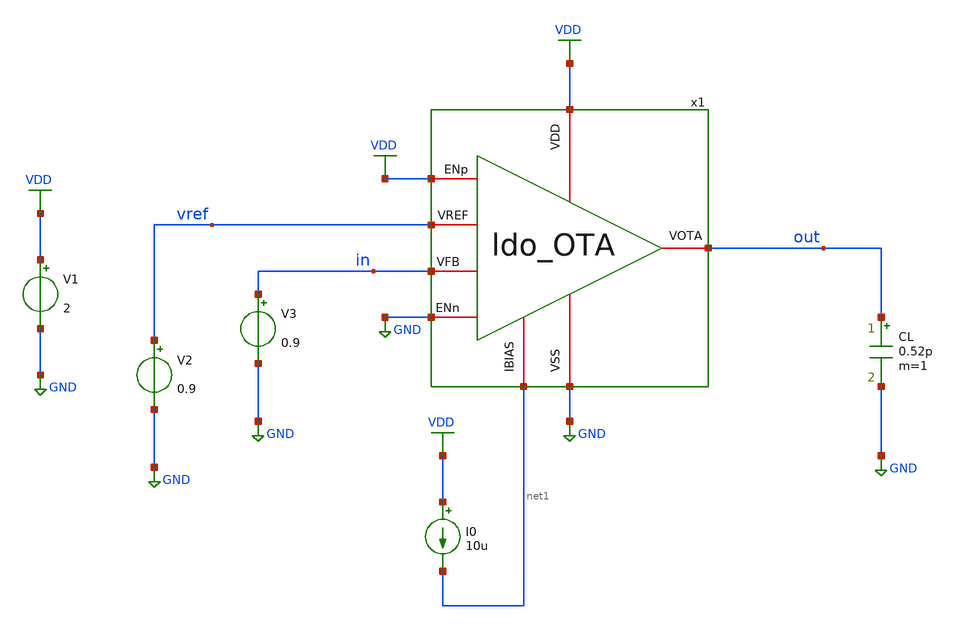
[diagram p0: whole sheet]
** sch_path: designs/libs/tb_ldo/tb_ldo_OTA_ac/tb_ldo_OTA_ac.sch
**.subckt tb_ldo_OTA_ac
V1 VDD GND 2
V2 vref GND 0.9
I0 VDD net1 10u
CL out GND 0.52p m=1
V3 in GND 0.9
x1 VDD vref in out net1 GND VDD GND ldo_OTA
**** begin user architecture code



.control
save all

** Set sources
alter @V3[AC] = 1

** Simulations
ac dec 100 1 10G

** Plots
setplot ac1
let gain_db = db(v(out))
plot gain_db
let phase_deg = cph(v(out))*180/pi
plot phase_deg

** Measurements
meas ac DC_gain FIND gain_db AT=1Hz
let gain_3db = DC_gain-3
meas ac f_3db WHEN gain_db=$&gain_3db
meas ac f_0db WHEN gain_db=0
meas ac phase_0db FIND phase_deg WHEN gain_db=0
let phase_margin = 180 + phase_0db
print phase_margin

write tb_ldo_OTA_ac.raw

.endc
* ngspice commands




.include $::180MCU_MODELS/design.ngspice
.lib $::180MCU_MODELS/sm141064.ngspice typical
.lib $::180MCU_MODELS/sm141064.ngspice cap_mim
.lib $::180MCU_MODELS/sm141064.ngspice moscap_typical
.lib $::180MCU_MODELS/sm141064.ngspice mimcap_typical
.lib $::180MCU_MODELS/sm141064.ngspice res_typical
* .lib $::180MCU_MODELS/sm141064.ngspice res_statistical
* ngspice commands

**** end user architecture code
**.ends

* expanding   symbol:  libs/core_ldo/ldo_OTA/ldo_OTA.sym # of pins=8
** sym_path: designs/libs/core_ldo/ldo_OTA/ldo_OTA.sym
** sch_path: designs/libs/core_ldo/ldo_OTA/ldo_OTA.sch
.subckt ldo_OTA VDD VREF VFB VOTA IBIAS VSS ENp ENn
*.iopin VDD
*.iopin VSS
*.iopin VOTA
*.iopin VREF
*.iopin IBIAS
*.iopin VFB
*.ipin ENp
*.ipin ENn
XM3 Vbp1 Vbp1 VDD VDD pfet_05v0 L=1.00u W=5.50u nf=1 ad='int((nf+1)/2) * W/nf * 0.18u' as='int((nf+2)/2) * W/nf * 0.18u'
+ pd='2*int((nf+1)/2) * (W/nf + 0.18u)' ps='2*int((nf+2)/2) * (W/nf + 0.18u)' nrd='0.18u / W' nrs='0.18u / W'
+ sa=0 sb=0 sd=0 m=2
XM4 Vbp2 Vbp2 VDD VDD pfet_05v0 L=1.00u W=5.50u nf=1 ad='int((nf+1)/2) * W/nf * 0.18u' as='int((nf+2)/2) * W/nf * 0.18u'
+ pd='2*int((nf+1)/2) * (W/nf + 0.18u)' ps='2*int((nf+2)/2) * (W/nf + 0.18u)' nrd='0.18u / W' nrs='0.18u / W'
+ sa=0 sb=0 sd=0 m=2
XM5 Vbn2 Vbp1 VDD VDD pfet_05v0 L=1.00u W=5.50u nf=1 ad='int((nf+1)/2) * W/nf * 0.18u' as='int((nf+2)/2) * W/nf * 0.18u'
+ pd='2*int((nf+1)/2) * (W/nf + 0.18u)' ps='2*int((nf+2)/2) * (W/nf + 0.18u)' nrd='0.18u / W' nrs='0.18u / W'
+ sa=0 sb=0 sd=0 m=2
XM6 VOTA Vbp2 VDD VDD pfet_05v0 L=1.00u W=5.50u nf=1 ad='int((nf+1)/2) * W/nf * 0.18u' as='int((nf+2)/2) * W/nf * 0.18u'
+ pd='2*int((nf+1)/2) * (W/nf + 0.18u)' ps='2*int((nf+2)/2) * (W/nf + 0.18u)' nrd='0.18u / W' nrs='0.18u / W'
+ sa=0 sb=0 sd=0 m=6
XM9 Vbn1 Vbn1 VSS VSS nfet_05v0 L=1.00u W=3.00u nf=1 ad='int((nf+1)/2) * W/nf * 0.18u' as='int((nf+2)/2) * W/nf * 0.18u'
+ pd='2*int((nf+1)/2) * (W/nf + 0.18u)' ps='2*int((nf+2)/2) * (W/nf + 0.18u)' nrd='0.18u / W' nrs='0.18u / W'
+ sa=0 sb=0 sd=0 m=2
XM10 Vtail Vbn1 VSS VSS nfet_05v0 L=1.00u W=3.00u nf=1 ad='int((nf+1)/2) * W/nf * 0.18u' as='int((nf+2)/2) * W/nf * 0.18u'
+ pd='2*int((nf+1)/2) * (W/nf + 0.18u)' ps='2*int((nf+2)/2) * (W/nf + 0.18u)' nrd='0.18u / W' nrs='0.18u / W'
+ sa=0 sb=0 sd=0 m=2
XM7 Vbn2 Vbn2 VSS VSS nfet_05v0 L=1.00u W=1.25u nf=1 ad='int((nf+1)/2) * W/nf * 0.18u' as='int((nf+2)/2) * W/nf * 0.18u'
+ pd='2*int((nf+1)/2) * (W/nf + 0.18u)' ps='2*int((nf+2)/2) * (W/nf + 0.18u)' nrd='0.18u / W' nrs='0.18u / W'
+ sa=0 sb=0 sd=0 m=2
XM8 VOTA Vbn2 VSS VSS nfet_05v0 L=1.00u W=1.25u nf=1 ad='int((nf+1)/2) * W/nf * 0.18u' as='int((nf+2)/2) * W/nf * 0.18u'
+ pd='2*int((nf+1)/2) * (W/nf + 0.18u)' ps='2*int((nf+2)/2) * (W/nf + 0.18u)' nrd='0.18u / W' nrs='0.18u / W'
+ sa=0 sb=0 sd=0 m=6
XM1 Vbp1 VREF Vtail VSS nfet_05v0 L=0.60u W=5.00u nf=1 ad='int((nf+1)/2) * W/nf * 0.18u' as='int((nf+2)/2) * W/nf * 0.18u'
+ pd='2*int((nf+1)/2) * (W/nf + 0.18u)' ps='2*int((nf+2)/2) * (W/nf + 0.18u)' nrd='0.18u / W' nrs='0.18u / W'
+ sa=0 sb=0 sd=0 m=14
XM2 Vbp2 VFB Vtail VSS nfet_05v0 L=0.60u W=5.00u nf=1 ad='int((nf+1)/2) * W/nf * 0.18u' as='int((nf+2)/2) * W/nf * 0.18u'
+ pd='2*int((nf+1)/2) * (W/nf + 0.18u)' ps='2*int((nf+2)/2) * (W/nf + 0.18u)' nrd='0.18u / W' nrs='0.18u / W'
+ sa=0 sb=0 sd=0 m=14
XMpota_dummy_L[3] VDD VDD VDD VDD pfet_05v0 L=1.00u W=5.50u nf=1 ad='int((nf+1)/2) * W/nf * 0.18u' as='int((nf+2)/2) * W/nf * 0.18u'
+ pd='2*int((nf+1)/2) * (W/nf + 0.18u)' ps='2*int((nf+2)/2) * (W/nf + 0.18u)' nrd='0.18u / W' nrs='0.18u / W'
+ sa=0 sb=0 sd=0 m=1
XMpota_dummy_L[2] VDD VDD VDD VDD pfet_05v0 L=1.00u W=5.50u nf=1 ad='int((nf+1)/2) * W/nf * 0.18u' as='int((nf+2)/2) * W/nf * 0.18u'
+ pd='2*int((nf+1)/2) * (W/nf + 0.18u)' ps='2*int((nf+2)/2) * (W/nf + 0.18u)' nrd='0.18u / W' nrs='0.18u / W'
+ sa=0 sb=0 sd=0 m=1
XMpota_dummy_L[1] VDD VDD VDD VDD pfet_05v0 L=1.00u W=5.50u nf=1 ad='int((nf+1)/2) * W/nf * 0.18u' as='int((nf+2)/2) * W/nf * 0.18u'
+ pd='2*int((nf+1)/2) * (W/nf + 0.18u)' ps='2*int((nf+2)/2) * (W/nf + 0.18u)' nrd='0.18u / W' nrs='0.18u / W'
+ sa=0 sb=0 sd=0 m=1
XMpota_dummy_L[0] VDD VDD VDD VDD pfet_05v0 L=1.00u W=5.50u nf=1 ad='int((nf+1)/2) * W/nf * 0.18u' as='int((nf+2)/2) * W/nf * 0.18u'
+ pd='2*int((nf+1)/2) * (W/nf + 0.18u)' ps='2*int((nf+2)/2) * (W/nf + 0.18u)' nrd='0.18u / W' nrs='0.18u / W'
+ sa=0 sb=0 sd=0 m=1
XMpota_dummy_TB[15] VDD VDD VDD VDD pfet_05v0 L=1.00u W=5.50u nf=1 ad='int((nf+1)/2) * W/nf * 0.18u'
+ as='int((nf+2)/2) * W/nf * 0.18u' pd='2*int((nf+1)/2) * (W/nf + 0.18u)' ps='2*int((nf+2)/2) * (W/nf + 0.18u)'
+ nrd='0.18u / W' nrs='0.18u / W' sa=0 sb=0 sd=0 m=1
XMpota_dummy_TB[14] VDD VDD VDD VDD pfet_05v0 L=1.00u W=5.50u nf=1 ad='int((nf+1)/2) * W/nf * 0.18u'
+ as='int((nf+2)/2) * W/nf * 0.18u' pd='2*int((nf+1)/2) * (W/nf + 0.18u)' ps='2*int((nf+2)/2) * (W/nf + 0.18u)'
+ nrd='0.18u / W' nrs='0.18u / W' sa=0 sb=0 sd=0 m=1
XMpota_dummy_TB[13] VDD VDD VDD VDD pfet_05v0 L=1.00u W=5.50u nf=1 ad='int((nf+1)/2) * W/nf * 0.18u'
+ as='int((nf+2)/2) * W/nf * 0.18u' pd='2*int((nf+1)/2) * (W/nf + 0.18u)' ps='2*int((nf+2)/2) * (W/nf + 0.18u)'
+ nrd='0.18u / W' nrs='0.18u / W' sa=0 sb=0 sd=0 m=1
XMpota_dummy_TB[12] VDD VDD VDD VDD pfet_05v0 L=1.00u W=5.50u nf=1 ad='int((nf+1)/2) * W/nf * 0.18u'
+ as='int((nf+2)/2) * W/nf * 0.18u' pd='2*int((nf+1)/2) * (W/nf + 0.18u)' ps='2*int((nf+2)/2) * (W/nf + 0.18u)'
+ nrd='0.18u / W' nrs='0.18u / W' sa=0 sb=0 sd=0 m=1
XMpota_dummy_TB[11] VDD VDD VDD VDD pfet_05v0 L=1.00u W=5.50u nf=1 ad='int((nf+1)/2) * W/nf * 0.18u'
+ as='int((nf+2)/2) * W/nf * 0.18u' pd='2*int((nf+1)/2) * (W/nf + 0.18u)' ps='2*int((nf+2)/2) * (W/nf + 0.18u)'
+ nrd='0.18u / W' nrs='0.18u / W' sa=0 sb=0 sd=0 m=1
XMpota_dummy_TB[10] VDD VDD VDD VDD pfet_05v0 L=1.00u W=5.50u nf=1 ad='int((nf+1)/2) * W/nf * 0.18u'
+ as='int((nf+2)/2) * W/nf * 0.18u' pd='2*int((nf+1)/2) * (W/nf + 0.18u)' ps='2*int((nf+2)/2) * (W/nf + 0.18u)'
+ nrd='0.18u / W' nrs='0.18u / W' sa=0 sb=0 sd=0 m=1
XMpota_dummy_TB[9] VDD VDD VDD VDD pfet_05v0 L=1.00u W=5.50u nf=1 ad='int((nf+1)/2) * W/nf * 0.18u' as='int((nf+2)/2) * W/nf * 0.18u'
+ pd='2*int((nf+1)/2) * (W/nf + 0.18u)' ps='2*int((nf+2)/2) * (W/nf + 0.18u)' nrd='0.18u / W' nrs='0.18u / W'
+ sa=0 sb=0 sd=0 m=1
XMpota_dummy_TB[8] VDD VDD VDD VDD pfet_05v0 L=1.00u W=5.50u nf=1 ad='int((nf+1)/2) * W/nf * 0.18u' as='int((nf+2)/2) * W/nf * 0.18u'
+ pd='2*int((nf+1)/2) * (W/nf + 0.18u)' ps='2*int((nf+2)/2) * (W/nf + 0.18u)' nrd='0.18u / W' nrs='0.18u / W'
+ sa=0 sb=0 sd=0 m=1
XMpota_dummy_TB[7] VDD VDD VDD VDD pfet_05v0 L=1.00u W=5.50u nf=1 ad='int((nf+1)/2) * W/nf * 0.18u' as='int((nf+2)/2) * W/nf * 0.18u'
+ pd='2*int((nf+1)/2) * (W/nf + 0.18u)' ps='2*int((nf+2)/2) * (W/nf + 0.18u)' nrd='0.18u / W' nrs='0.18u / W'
+ sa=0 sb=0 sd=0 m=1
XMpota_dummy_TB[6] VDD VDD VDD VDD pfet_05v0 L=1.00u W=5.50u nf=1 ad='int((nf+1)/2) * W/nf * 0.18u' as='int((nf+2)/2) * W/nf * 0.18u'
+ pd='2*int((nf+1)/2) * (W/nf + 0.18u)' ps='2*int((nf+2)/2) * (W/nf + 0.18u)' nrd='0.18u / W' nrs='0.18u / W'
+ sa=0 sb=0 sd=0 m=1
XMpota_dummy_TB[5] VDD VDD VDD VDD pfet_05v0 L=1.00u W=5.50u nf=1 ad='int((nf+1)/2) * W/nf * 0.18u' as='int((nf+2)/2) * W/nf * 0.18u'
+ pd='2*int((nf+1)/2) * (W/nf + 0.18u)' ps='2*int((nf+2)/2) * (W/nf + 0.18u)' nrd='0.18u / W' nrs='0.18u / W'
+ sa=0 sb=0 sd=0 m=1
XMpota_dummy_TB[4] VDD VDD VDD VDD pfet_05v0 L=1.00u W=5.50u nf=1 ad='int((nf+1)/2) * W/nf * 0.18u' as='int((nf+2)/2) * W/nf * 0.18u'
+ pd='2*int((nf+1)/2) * (W/nf + 0.18u)' ps='2*int((nf+2)/2) * (W/nf + 0.18u)' nrd='0.18u / W' nrs='0.18u / W'
+ sa=0 sb=0 sd=0 m=1
XMpota_dummy_TB[3] VDD VDD VDD VDD pfet_05v0 L=1.00u W=5.50u nf=1 ad='int((nf+1)/2) * W/nf * 0.18u' as='int((nf+2)/2) * W/nf * 0.18u'
+ pd='2*int((nf+1)/2) * (W/nf + 0.18u)' ps='2*int((nf+2)/2) * (W/nf + 0.18u)' nrd='0.18u / W' nrs='0.18u / W'
+ sa=0 sb=0 sd=0 m=1
XMpota_dummy_TB[2] VDD VDD VDD VDD pfet_05v0 L=1.00u W=5.50u nf=1 ad='int((nf+1)/2) * W/nf * 0.18u' as='int((nf+2)/2) * W/nf * 0.18u'
+ pd='2*int((nf+1)/2) * (W/nf + 0.18u)' ps='2*int((nf+2)/2) * (W/nf + 0.18u)' nrd='0.18u / W' nrs='0.18u / W'
+ sa=0 sb=0 sd=0 m=1
XMpota_dummy_TB[1] VDD VDD VDD VDD pfet_05v0 L=1.00u W=5.50u nf=1 ad='int((nf+1)/2) * W/nf * 0.18u' as='int((nf+2)/2) * W/nf * 0.18u'
+ pd='2*int((nf+1)/2) * (W/nf + 0.18u)' ps='2*int((nf+2)/2) * (W/nf + 0.18u)' nrd='0.18u / W' nrs='0.18u / W'
+ sa=0 sb=0 sd=0 m=1
XMpota_dummy_TB[0] VDD VDD VDD VDD pfet_05v0 L=1.00u W=5.50u nf=1 ad='int((nf+1)/2) * W/nf * 0.18u' as='int((nf+2)/2) * W/nf * 0.18u'
+ pd='2*int((nf+1)/2) * (W/nf + 0.18u)' ps='2*int((nf+2)/2) * (W/nf + 0.18u)' nrd='0.18u / W' nrs='0.18u / W'
+ sa=0 sb=0 sd=0 m=1
XMndiff_dummy_L[7] VSS VSS VSS VSS nfet_05v0 L=0.60u W=5.00u nf=1 ad='int((nf+1)/2) * W/nf * 0.18u' as='int((nf+2)/2) * W/nf * 0.18u'
+ pd='2*int((nf+1)/2) * (W/nf + 0.18u)' ps='2*int((nf+2)/2) * (W/nf + 0.18u)' nrd='0.18u / W' nrs='0.18u / W'
+ sa=0 sb=0 sd=0 m=1
XMndiff_dummy_L[6] VSS VSS VSS VSS nfet_05v0 L=0.60u W=5.00u nf=1 ad='int((nf+1)/2) * W/nf * 0.18u' as='int((nf+2)/2) * W/nf * 0.18u'
+ pd='2*int((nf+1)/2) * (W/nf + 0.18u)' ps='2*int((nf+2)/2) * (W/nf + 0.18u)' nrd='0.18u / W' nrs='0.18u / W'
+ sa=0 sb=0 sd=0 m=1
XMndiff_dummy_L[5] VSS VSS VSS VSS nfet_05v0 L=0.60u W=5.00u nf=1 ad='int((nf+1)/2) * W/nf * 0.18u' as='int((nf+2)/2) * W/nf * 0.18u'
+ pd='2*int((nf+1)/2) * (W/nf + 0.18u)' ps='2*int((nf+2)/2) * (W/nf + 0.18u)' nrd='0.18u / W' nrs='0.18u / W'
+ sa=0 sb=0 sd=0 m=1
XMndiff_dummy_L[4] VSS VSS VSS VSS nfet_05v0 L=0.60u W=5.00u nf=1 ad='int((nf+1)/2) * W/nf * 0.18u' as='int((nf+2)/2) * W/nf * 0.18u'
+ pd='2*int((nf+1)/2) * (W/nf + 0.18u)' ps='2*int((nf+2)/2) * (W/nf + 0.18u)' nrd='0.18u / W' nrs='0.18u / W'
+ sa=0 sb=0 sd=0 m=1
XMndiff_dummy_L[3] VSS VSS VSS VSS nfet_05v0 L=0.60u W=5.00u nf=1 ad='int((nf+1)/2) * W/nf * 0.18u' as='int((nf+2)/2) * W/nf * 0.18u'
+ pd='2*int((nf+1)/2) * (W/nf + 0.18u)' ps='2*int((nf+2)/2) * (W/nf + 0.18u)' nrd='0.18u / W' nrs='0.18u / W'
+ sa=0 sb=0 sd=0 m=1
XMndiff_dummy_L[2] VSS VSS VSS VSS nfet_05v0 L=0.60u W=5.00u nf=1 ad='int((nf+1)/2) * W/nf * 0.18u' as='int((nf+2)/2) * W/nf * 0.18u'
+ pd='2*int((nf+1)/2) * (W/nf + 0.18u)' ps='2*int((nf+2)/2) * (W/nf + 0.18u)' nrd='0.18u / W' nrs='0.18u / W'
+ sa=0 sb=0 sd=0 m=1
XMndiff_dummy_L[1] VSS VSS VSS VSS nfet_05v0 L=0.60u W=5.00u nf=1 ad='int((nf+1)/2) * W/nf * 0.18u' as='int((nf+2)/2) * W/nf * 0.18u'
+ pd='2*int((nf+1)/2) * (W/nf + 0.18u)' ps='2*int((nf+2)/2) * (W/nf + 0.18u)' nrd='0.18u / W' nrs='0.18u / W'
+ sa=0 sb=0 sd=0 m=1
XMndiff_dummy_L[0] VSS VSS VSS VSS nfet_05v0 L=0.60u W=5.00u nf=1 ad='int((nf+1)/2) * W/nf * 0.18u' as='int((nf+2)/2) * W/nf * 0.18u'
+ pd='2*int((nf+1)/2) * (W/nf + 0.18u)' ps='2*int((nf+2)/2) * (W/nf + 0.18u)' nrd='0.18u / W' nrs='0.18u / W'
+ sa=0 sb=0 sd=0 m=1
XMndiff_dummy_TB[17] VSS VSS VSS VSS nfet_05v0 L=0.60u W=5.00u nf=1 ad='int((nf+1)/2) * W/nf * 0.18u'
+ as='int((nf+2)/2) * W/nf * 0.18u' pd='2*int((nf+1)/2) * (W/nf + 0.18u)' ps='2*int((nf+2)/2) * (W/nf + 0.18u)'
+ nrd='0.18u / W' nrs='0.18u / W' sa=0 sb=0 sd=0 m=1
XMndiff_dummy_TB[16] VSS VSS VSS VSS nfet_05v0 L=0.60u W=5.00u nf=1 ad='int((nf+1)/2) * W/nf * 0.18u'
+ as='int((nf+2)/2) * W/nf * 0.18u' pd='2*int((nf+1)/2) * (W/nf + 0.18u)' ps='2*int((nf+2)/2) * (W/nf + 0.18u)'
+ nrd='0.18u / W' nrs='0.18u / W' sa=0 sb=0 sd=0 m=1
XMndiff_dummy_TB[15] VSS VSS VSS VSS nfet_05v0 L=0.60u W=5.00u nf=1 ad='int((nf+1)/2) * W/nf * 0.18u'
+ as='int((nf+2)/2) * W/nf * 0.18u' pd='2*int((nf+1)/2) * (W/nf + 0.18u)' ps='2*int((nf+2)/2) * (W/nf + 0.18u)'
+ nrd='0.18u / W' nrs='0.18u / W' sa=0 sb=0 sd=0 m=1
XMndiff_dummy_TB[14] VSS VSS VSS VSS nfet_05v0 L=0.60u W=5.00u nf=1 ad='int((nf+1)/2) * W/nf * 0.18u'
+ as='int((nf+2)/2) * W/nf * 0.18u' pd='2*int((nf+1)/2) * (W/nf + 0.18u)' ps='2*int((nf+2)/2) * (W/nf + 0.18u)'
+ nrd='0.18u / W' nrs='0.18u / W' sa=0 sb=0 sd=0 m=1
XMndiff_dummy_TB[13] VSS VSS VSS VSS nfet_05v0 L=0.60u W=5.00u nf=1 ad='int((nf+1)/2) * W/nf * 0.18u'
+ as='int((nf+2)/2) * W/nf * 0.18u' pd='2*int((nf+1)/2) * (W/nf + 0.18u)' ps='2*int((nf+2)/2) * (W/nf + 0.18u)'
+ nrd='0.18u / W' nrs='0.18u / W' sa=0 sb=0 sd=0 m=1
XMndiff_dummy_TB[12] VSS VSS VSS VSS nfet_05v0 L=0.60u W=5.00u nf=1 ad='int((nf+1)/2) * W/nf * 0.18u'
+ as='int((nf+2)/2) * W/nf * 0.18u' pd='2*int((nf+1)/2) * (W/nf + 0.18u)' ps='2*int((nf+2)/2) * (W/nf + 0.18u)'
+ nrd='0.18u / W' nrs='0.18u / W' sa=0 sb=0 sd=0 m=1
XMndiff_dummy_TB[11] VSS VSS VSS VSS nfet_05v0 L=0.60u W=5.00u nf=1 ad='int((nf+1)/2) * W/nf * 0.18u'
+ as='int((nf+2)/2) * W/nf * 0.18u' pd='2*int((nf+1)/2) * (W/nf + 0.18u)' ps='2*int((nf+2)/2) * (W/nf + 0.18u)'
+ nrd='0.18u / W' nrs='0.18u / W' sa=0 sb=0 sd=0 m=1
XMndiff_dummy_TB[10] VSS VSS VSS VSS nfet_05v0 L=0.60u W=5.00u nf=1 ad='int((nf+1)/2) * W/nf * 0.18u'
+ as='int((nf+2)/2) * W/nf * 0.18u' pd='2*int((nf+1)/2) * (W/nf + 0.18u)' ps='2*int((nf+2)/2) * (W/nf + 0.18u)'
+ nrd='0.18u / W' nrs='0.18u / W' sa=0 sb=0 sd=0 m=1
XMndiff_dummy_TB[9] VSS VSS VSS VSS nfet_05v0 L=0.60u W=5.00u nf=1 ad='int((nf+1)/2) * W/nf * 0.18u'
+ as='int((nf+2)/2) * W/nf * 0.18u' pd='2*int((nf+1)/2) * (W/nf + 0.18u)' ps='2*int((nf+2)/2) * (W/nf + 0.18u)'
+ nrd='0.18u / W' nrs='0.18u / W' sa=0 sb=0 sd=0 m=1
XMndiff_dummy_TB[8] VSS VSS VSS VSS nfet_05v0 L=0.60u W=5.00u nf=1 ad='int((nf+1)/2) * W/nf * 0.18u'
+ as='int((nf+2)/2) * W/nf * 0.18u' pd='2*int((nf+1)/2) * (W/nf + 0.18u)' ps='2*int((nf+2)/2) * (W/nf + 0.18u)'
+ nrd='0.18u / W' nrs='0.18u / W' sa=0 sb=0 sd=0 m=1
XMndiff_dummy_TB[7] VSS VSS VSS VSS nfet_05v0 L=0.60u W=5.00u nf=1 ad='int((nf+1)/2) * W/nf * 0.18u'
+ as='int((nf+2)/2) * W/nf * 0.18u' pd='2*int((nf+1)/2) * (W/nf + 0.18u)' ps='2*int((nf+2)/2) * (W/nf + 0.18u)'
+ nrd='0.18u / W' nrs='0.18u / W' sa=0 sb=0 sd=0 m=1
XMndiff_dummy_TB[6] VSS VSS VSS VSS nfet_05v0 L=0.60u W=5.00u nf=1 ad='int((nf+1)/2) * W/nf * 0.18u'
+ as='int((nf+2)/2) * W/nf * 0.18u' pd='2*int((nf+1)/2) * (W/nf + 0.18u)' ps='2*int((nf+2)/2) * (W/nf + 0.18u)'
+ nrd='0.18u / W' nrs='0.18u / W' sa=0 sb=0 sd=0 m=1
XMndiff_dummy_TB[5] VSS VSS VSS VSS nfet_05v0 L=0.60u W=5.00u nf=1 ad='int((nf+1)/2) * W/nf * 0.18u'
+ as='int((nf+2)/2) * W/nf * 0.18u' pd='2*int((nf+1)/2) * (W/nf + 0.18u)' ps='2*int((nf+2)/2) * (W/nf + 0.18u)'
+ nrd='0.18u / W' nrs='0.18u / W' sa=0 sb=0 sd=0 m=1
XMndiff_dummy_TB[4] VSS VSS VSS VSS nfet_05v0 L=0.60u W=5.00u nf=1 ad='int((nf+1)/2) * W/nf * 0.18u'
+ as='int((nf+2)/2) * W/nf * 0.18u' pd='2*int((nf+1)/2) * (W/nf + 0.18u)' ps='2*int((nf+2)/2) * (W/nf + 0.18u)'
+ nrd='0.18u / W' nrs='0.18u / W' sa=0 sb=0 sd=0 m=1
XMndiff_dummy_TB[3] VSS VSS VSS VSS nfet_05v0 L=0.60u W=5.00u nf=1 ad='int((nf+1)/2) * W/nf * 0.18u'
+ as='int((nf+2)/2) * W/nf * 0.18u' pd='2*int((nf+1)/2) * (W/nf + 0.18u)' ps='2*int((nf+2)/2) * (W/nf + 0.18u)'
+ nrd='0.18u / W' nrs='0.18u / W' sa=0 sb=0 sd=0 m=1
XMndiff_dummy_TB[2] VSS VSS VSS VSS nfet_05v0 L=0.60u W=5.00u nf=1 ad='int((nf+1)/2) * W/nf * 0.18u'
+ as='int((nf+2)/2) * W/nf * 0.18u' pd='2*int((nf+1)/2) * (W/nf + 0.18u)' ps='2*int((nf+2)/2) * (W/nf + 0.18u)'
+ nrd='0.18u / W' nrs='0.18u / W' sa=0 sb=0 sd=0 m=1
XMndiff_dummy_TB[1] VSS VSS VSS VSS nfet_05v0 L=0.60u W=5.00u nf=1 ad='int((nf+1)/2) * W/nf * 0.18u'
+ as='int((nf+2)/2) * W/nf * 0.18u' pd='2*int((nf+1)/2) * (W/nf + 0.18u)' ps='2*int((nf+2)/2) * (W/nf + 0.18u)'
+ nrd='0.18u / W' nrs='0.18u / W' sa=0 sb=0 sd=0 m=1
XMndiff_dummy_TB[0] VSS VSS VSS VSS nfet_05v0 L=0.60u W=5.00u nf=1 ad='int((nf+1)/2) * W/nf * 0.18u'
+ as='int((nf+2)/2) * W/nf * 0.18u' pd='2*int((nf+1)/2) * (W/nf + 0.18u)' ps='2*int((nf+2)/2) * (W/nf + 0.18u)'
+ nrd='0.18u / W' nrs='0.18u / W' sa=0 sb=0 sd=0 m=1
XMnota_dummy_L[3] VSS VSS VSS VSS nfet_05v0 L=1.00u W=1.25u nf=1 ad='int((nf+1)/2) * W/nf * 0.18u' as='int((nf+2)/2) * W/nf * 0.18u'
+ pd='2*int((nf+1)/2) * (W/nf + 0.18u)' ps='2*int((nf+2)/2) * (W/nf + 0.18u)' nrd='0.18u / W' nrs='0.18u / W'
+ sa=0 sb=0 sd=0 m=1
XMnota_dummy_L[2] VSS VSS VSS VSS nfet_05v0 L=1.00u W=1.25u nf=1 ad='int((nf+1)/2) * W/nf * 0.18u' as='int((nf+2)/2) * W/nf * 0.18u'
+ pd='2*int((nf+1)/2) * (W/nf + 0.18u)' ps='2*int((nf+2)/2) * (W/nf + 0.18u)' nrd='0.18u / W' nrs='0.18u / W'
+ sa=0 sb=0 sd=0 m=1
XMnota_dummy_L[1] VSS VSS VSS VSS nfet_05v0 L=1.00u W=1.25u nf=1 ad='int((nf+1)/2) * W/nf * 0.18u' as='int((nf+2)/2) * W/nf * 0.18u'
+ pd='2*int((nf+1)/2) * (W/nf + 0.18u)' ps='2*int((nf+2)/2) * (W/nf + 0.18u)' nrd='0.18u / W' nrs='0.18u / W'
+ sa=0 sb=0 sd=0 m=1
XMnota_dummy_L[0] VSS VSS VSS VSS nfet_05v0 L=1.00u W=1.25u nf=1 ad='int((nf+1)/2) * W/nf * 0.18u' as='int((nf+2)/2) * W/nf * 0.18u'
+ pd='2*int((nf+1)/2) * (W/nf + 0.18u)' ps='2*int((nf+2)/2) * (W/nf + 0.18u)' nrd='0.18u / W' nrs='0.18u / W'
+ sa=0 sb=0 sd=0 m=1
XMnota_dummy_TB[11] VSS VSS VSS VSS nfet_05v0 L=1.00u W=1.25u nf=1 ad='int((nf+1)/2) * W/nf * 0.18u'
+ as='int((nf+2)/2) * W/nf * 0.18u' pd='2*int((nf+1)/2) * (W/nf + 0.18u)' ps='2*int((nf+2)/2) * (W/nf + 0.18u)'
+ nrd='0.18u / W' nrs='0.18u / W' sa=0 sb=0 sd=0 m=1
XMnota_dummy_TB[10] VSS VSS VSS VSS nfet_05v0 L=1.00u W=1.25u nf=1 ad='int((nf+1)/2) * W/nf * 0.18u'
+ as='int((nf+2)/2) * W/nf * 0.18u' pd='2*int((nf+1)/2) * (W/nf + 0.18u)' ps='2*int((nf+2)/2) * (W/nf + 0.18u)'
+ nrd='0.18u / W' nrs='0.18u / W' sa=0 sb=0 sd=0 m=1
XMnota_dummy_TB[9] VSS VSS VSS VSS nfet_05v0 L=1.00u W=1.25u nf=1 ad='int((nf+1)/2) * W/nf * 0.18u' as='int((nf+2)/2) * W/nf * 0.18u'
+ pd='2*int((nf+1)/2) * (W/nf + 0.18u)' ps='2*int((nf+2)/2) * (W/nf + 0.18u)' nrd='0.18u / W' nrs='0.18u / W'
+ sa=0 sb=0 sd=0 m=1
XMnota_dummy_TB[8] VSS VSS VSS VSS nfet_05v0 L=1.00u W=1.25u nf=1 ad='int((nf+1)/2) * W/nf * 0.18u' as='int((nf+2)/2) * W/nf * 0.18u'
+ pd='2*int((nf+1)/2) * (W/nf + 0.18u)' ps='2*int((nf+2)/2) * (W/nf + 0.18u)' nrd='0.18u / W' nrs='0.18u / W'
+ sa=0 sb=0 sd=0 m=1
XMnota_dummy_TB[7] VSS VSS VSS VSS nfet_05v0 L=1.00u W=1.25u nf=1 ad='int((nf+1)/2) * W/nf * 0.18u' as='int((nf+2)/2) * W/nf * 0.18u'
+ pd='2*int((nf+1)/2) * (W/nf + 0.18u)' ps='2*int((nf+2)/2) * (W/nf + 0.18u)' nrd='0.18u / W' nrs='0.18u / W'
+ sa=0 sb=0 sd=0 m=1
XMnota_dummy_TB[6] VSS VSS VSS VSS nfet_05v0 L=1.00u W=1.25u nf=1 ad='int((nf+1)/2) * W/nf * 0.18u' as='int((nf+2)/2) * W/nf * 0.18u'
+ pd='2*int((nf+1)/2) * (W/nf + 0.18u)' ps='2*int((nf+2)/2) * (W/nf + 0.18u)' nrd='0.18u / W' nrs='0.18u / W'
+ sa=0 sb=0 sd=0 m=1
XMnota_dummy_TB[5] VSS VSS VSS VSS nfet_05v0 L=1.00u W=1.25u nf=1 ad='int((nf+1)/2) * W/nf * 0.18u' as='int((nf+2)/2) * W/nf * 0.18u'
+ pd='2*int((nf+1)/2) * (W/nf + 0.18u)' ps='2*int((nf+2)/2) * (W/nf + 0.18u)' nrd='0.18u / W' nrs='0.18u / W'
+ sa=0 sb=0 sd=0 m=1
XMnota_dummy_TB[4] VSS VSS VSS VSS nfet_05v0 L=1.00u W=1.25u nf=1 ad='int((nf+1)/2) * W/nf * 0.18u' as='int((nf+2)/2) * W/nf * 0.18u'
+ pd='2*int((nf+1)/2) * (W/nf + 0.18u)' ps='2*int((nf+2)/2) * (W/nf + 0.18u)' nrd='0.18u / W' nrs='0.18u / W'
+ sa=0 sb=0 sd=0 m=1
XMnota_dummy_TB[3] VSS VSS VSS VSS nfet_05v0 L=1.00u W=1.25u nf=1 ad='int((nf+1)/2) * W/nf * 0.18u' as='int((nf+2)/2) * W/nf * 0.18u'
+ pd='2*int((nf+1)/2) * (W/nf + 0.18u)' ps='2*int((nf+2)/2) * (W/nf + 0.18u)' nrd='0.18u / W' nrs='0.18u / W'
+ sa=0 sb=0 sd=0 m=1
XMnota_dummy_TB[2] VSS VSS VSS VSS nfet_05v0 L=1.00u W=1.25u nf=1 ad='int((nf+1)/2) * W/nf * 0.18u' as='int((nf+2)/2) * W/nf * 0.18u'
+ pd='2*int((nf+1)/2) * (W/nf + 0.18u)' ps='2*int((nf+2)/2) * (W/nf + 0.18u)' nrd='0.18u / W' nrs='0.18u / W'
+ sa=0 sb=0 sd=0 m=1
XMnota_dummy_TB[1] VSS VSS VSS VSS nfet_05v0 L=1.00u W=1.25u nf=1 ad='int((nf+1)/2) * W/nf * 0.18u' as='int((nf+2)/2) * W/nf * 0.18u'
+ pd='2*int((nf+1)/2) * (W/nf + 0.18u)' ps='2*int((nf+2)/2) * (W/nf + 0.18u)' nrd='0.18u / W' nrs='0.18u / W'
+ sa=0 sb=0 sd=0 m=1
XMnota_dummy_TB[0] VSS VSS VSS VSS nfet_05v0 L=1.00u W=1.25u nf=1 ad='int((nf+1)/2) * W/nf * 0.18u' as='int((nf+2)/2) * W/nf * 0.18u'
+ pd='2*int((nf+1)/2) * (W/nf + 0.18u)' ps='2*int((nf+2)/2) * (W/nf + 0.18u)' nrd='0.18u / W' nrs='0.18u / W'
+ sa=0 sb=0 sd=0 m=1
XMnbias_dummy_L[3] VSS VSS VSS VSS nfet_05v0 L=1.00u W=3.00u nf=1 ad='int((nf+1)/2) * W/nf * 0.18u' as='int((nf+2)/2) * W/nf * 0.18u'
+ pd='2*int((nf+1)/2) * (W/nf + 0.18u)' ps='2*int((nf+2)/2) * (W/nf + 0.18u)' nrd='0.18u / W' nrs='0.18u / W'
+ sa=0 sb=0 sd=0 m=1
XMnbias_dummy_L[2] VSS VSS VSS VSS nfet_05v0 L=1.00u W=3.00u nf=1 ad='int((nf+1)/2) * W/nf * 0.18u' as='int((nf+2)/2) * W/nf * 0.18u'
+ pd='2*int((nf+1)/2) * (W/nf + 0.18u)' ps='2*int((nf+2)/2) * (W/nf + 0.18u)' nrd='0.18u / W' nrs='0.18u / W'
+ sa=0 sb=0 sd=0 m=1
XMnbias_dummy_L[1] VSS VSS VSS VSS nfet_05v0 L=1.00u W=3.00u nf=1 ad='int((nf+1)/2) * W/nf * 0.18u' as='int((nf+2)/2) * W/nf * 0.18u'
+ pd='2*int((nf+1)/2) * (W/nf + 0.18u)' ps='2*int((nf+2)/2) * (W/nf + 0.18u)' nrd='0.18u / W' nrs='0.18u / W'
+ sa=0 sb=0 sd=0 m=1
XMnbias_dummy_L[0] VSS VSS VSS VSS nfet_05v0 L=1.00u W=3.00u nf=1 ad='int((nf+1)/2) * W/nf * 0.18u' as='int((nf+2)/2) * W/nf * 0.18u'
+ pd='2*int((nf+1)/2) * (W/nf + 0.18u)' ps='2*int((nf+2)/2) * (W/nf + 0.18u)' nrd='0.18u / W' nrs='0.18u / W'
+ sa=0 sb=0 sd=0 m=1
XMnbias_dummy_TB[7] VSS VSS VSS VSS nfet_05v0 L=1.00u W=3.00u nf=1 ad='int((nf+1)/2) * W/nf * 0.18u'
+ as='int((nf+2)/2) * W/nf * 0.18u' pd='2*int((nf+1)/2) * (W/nf + 0.18u)' ps='2*int((nf+2)/2) * (W/nf + 0.18u)'
+ nrd='0.18u / W' nrs='0.18u / W' sa=0 sb=0 sd=0 m=1
XMnbias_dummy_TB[6] VSS VSS VSS VSS nfet_05v0 L=1.00u W=3.00u nf=1 ad='int((nf+1)/2) * W/nf * 0.18u'
+ as='int((nf+2)/2) * W/nf * 0.18u' pd='2*int((nf+1)/2) * (W/nf + 0.18u)' ps='2*int((nf+2)/2) * (W/nf + 0.18u)'
+ nrd='0.18u / W' nrs='0.18u / W' sa=0 sb=0 sd=0 m=1
XMnbias_dummy_TB[5] VSS VSS VSS VSS nfet_05v0 L=1.00u W=3.00u nf=1 ad='int((nf+1)/2) * W/nf * 0.18u'
+ as='int((nf+2)/2) * W/nf * 0.18u' pd='2*int((nf+1)/2) * (W/nf + 0.18u)' ps='2*int((nf+2)/2) * (W/nf + 0.18u)'
+ nrd='0.18u / W' nrs='0.18u / W' sa=0 sb=0 sd=0 m=1
XMnbias_dummy_TB[4] VSS VSS VSS VSS nfet_05v0 L=1.00u W=3.00u nf=1 ad='int((nf+1)/2) * W/nf * 0.18u'
+ as='int((nf+2)/2) * W/nf * 0.18u' pd='2*int((nf+1)/2) * (W/nf + 0.18u)' ps='2*int((nf+2)/2) * (W/nf + 0.18u)'
+ nrd='0.18u / W' nrs='0.18u / W' sa=0 sb=0 sd=0 m=1
XMnbias_dummy_TB[3] VSS VSS VSS VSS nfet_05v0 L=1.00u W=3.00u nf=1 ad='int((nf+1)/2) * W/nf * 0.18u'
+ as='int((nf+2)/2) * W/nf * 0.18u' pd='2*int((nf+1)/2) * (W/nf + 0.18u)' ps='2*int((nf+2)/2) * (W/nf + 0.18u)'
+ nrd='0.18u / W' nrs='0.18u / W' sa=0 sb=0 sd=0 m=1
XMnbias_dummy_TB[2] VSS VSS VSS VSS nfet_05v0 L=1.00u W=3.00u nf=1 ad='int((nf+1)/2) * W/nf * 0.18u'
+ as='int((nf+2)/2) * W/nf * 0.18u' pd='2*int((nf+1)/2) * (W/nf + 0.18u)' ps='2*int((nf+2)/2) * (W/nf + 0.18u)'
+ nrd='0.18u / W' nrs='0.18u / W' sa=0 sb=0 sd=0 m=1
XMnbias_dummy_TB[1] VSS VSS VSS VSS nfet_05v0 L=1.00u W=3.00u nf=1 ad='int((nf+1)/2) * W/nf * 0.18u'
+ as='int((nf+2)/2) * W/nf * 0.18u' pd='2*int((nf+1)/2) * (W/nf + 0.18u)' ps='2*int((nf+2)/2) * (W/nf + 0.18u)'
+ nrd='0.18u / W' nrs='0.18u / W' sa=0 sb=0 sd=0 m=1
XMnbias_dummy_TB[0] VSS VSS VSS VSS nfet_05v0 L=1.00u W=3.00u nf=1 ad='int((nf+1)/2) * W/nf * 0.18u'
+ as='int((nf+2)/2) * W/nf * 0.18u' pd='2*int((nf+1)/2) * (W/nf + 0.18u)' ps='2*int((nf+2)/2) * (W/nf + 0.18u)'
+ nrd='0.18u / W' nrs='0.18u / W' sa=0 sb=0 sd=0 m=1
XMpenota1 Vbp2 ENp VDD VDD pfet_05v0 L=0.5u W=2u nf=1 ad='int((nf+1)/2) * W/nf * 0.18u' as='int((nf+2)/2) * W/nf * 0.18u'
+ pd='2*int((nf+1)/2) * (W/nf + 0.18u)' ps='2*int((nf+2)/2) * (W/nf + 0.18u)' nrd='0.18u / W' nrs='0.18u / W'
+ sa=0 sb=0 sd=0 m=1
XMpenota2 Vbp1 ENp VDD VDD pfet_05v0 L=0.5u W=2u nf=1 ad='int((nf+1)/2) * W/nf * 0.18u' as='int((nf+2)/2) * W/nf * 0.18u'
+ pd='2*int((nf+1)/2) * (W/nf + 0.18u)' ps='2*int((nf+2)/2) * (W/nf + 0.18u)' nrd='0.18u / W' nrs='0.18u / W'
+ sa=0 sb=0 sd=0 m=1
XMnenota1 Vbn2 ENn VSS VSS nfet_05v0 L=0.6u W=2u nf=1 ad='int((nf+1)/2) * W/nf * 0.18u' as='int((nf+2)/2) * W/nf * 0.18u'
+ pd='2*int((nf+1)/2) * (W/nf + 0.18u)' ps='2*int((nf+2)/2) * (W/nf + 0.18u)' nrd='0.18u / W' nrs='0.18u / W'
+ sa=0 sb=0 sd=0 m=1
XMnenota2 Vbn1 ENn VSS VSS nfet_05v0 L=0.6u W=2u nf=1 ad='int((nf+1)/2) * W/nf * 0.18u' as='int((nf+2)/2) * W/nf * 0.18u'
+ pd='2*int((nf+1)/2) * (W/nf + 0.18u)' ps='2*int((nf+2)/2) * (W/nf + 0.18u)' nrd='0.18u / W' nrs='0.18u / W'
+ sa=0 sb=0 sd=0 m=1
XMnenota3 IBIAS ENp Vbn1 VSS nfet_05v0 L=0.6u W=2u nf=1 ad='int((nf+1)/2) * W/nf * 0.18u' as='int((nf+2)/2) * W/nf * 0.18u'
+ pd='2*int((nf+1)/2) * (W/nf + 0.18u)' ps='2*int((nf+2)/2) * (W/nf + 0.18u)' nrd='0.18u / W' nrs='0.18u / W'
+ sa=0 sb=0 sd=0 m=1
.ends

.GLOBAL GND
.GLOBAL VDD
.end
